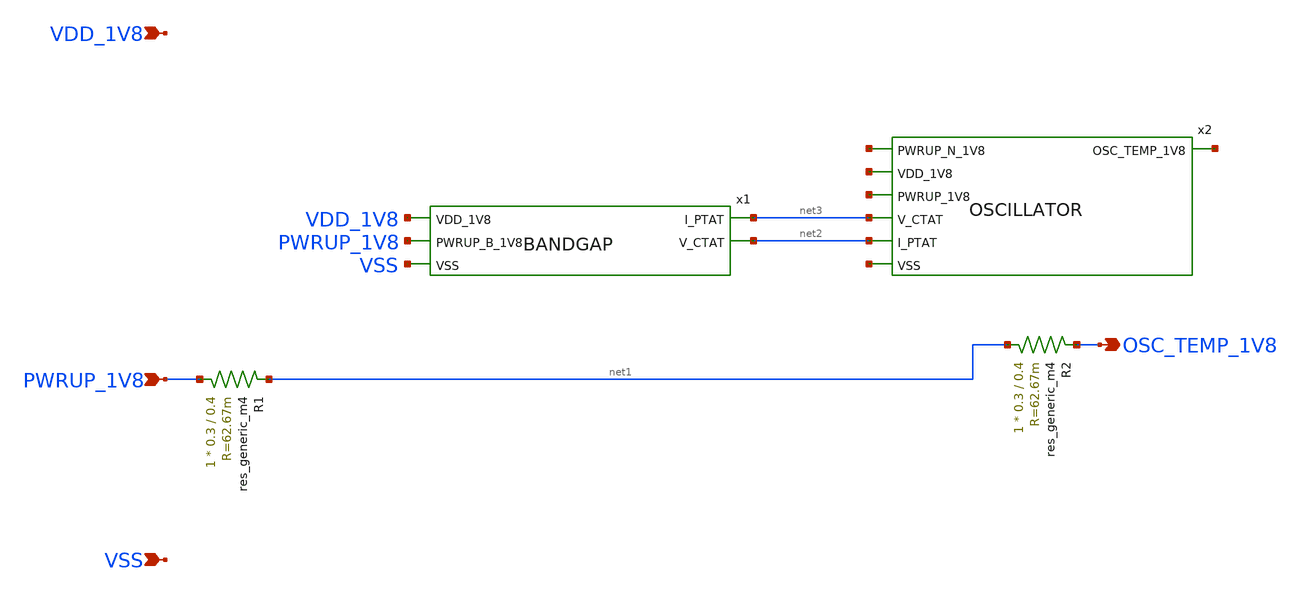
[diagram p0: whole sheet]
** sch_path: design/LELO_GR02_SKY130A/LELO_GR02.sch
**.subckt LELO_GR02 VDD_1V8 VSS PWRUP_1V8 OSC_TEMP_1V8
*.ipin VDD_1V8
*.ipin VSS
*.ipin PWRUP_1V8
*.opin OSC_TEMP_1V8
R2 net1 OSC_TEMP_1V8 sky130_fd_pr__res_generic_m4 W=0.3 L=0.4 m=1
R1 PWRUP_1V8 net1 sky130_fd_pr__res_generic_m4 W=0.3 L=0.4 m=1
x1 VDD_1V8 net3 net2 PWRUP_1V8 VSS BANDGAP
x2 net4 net5 net6 net7 net3 net2 net8 OSCILLATOR
**.ends
.end
